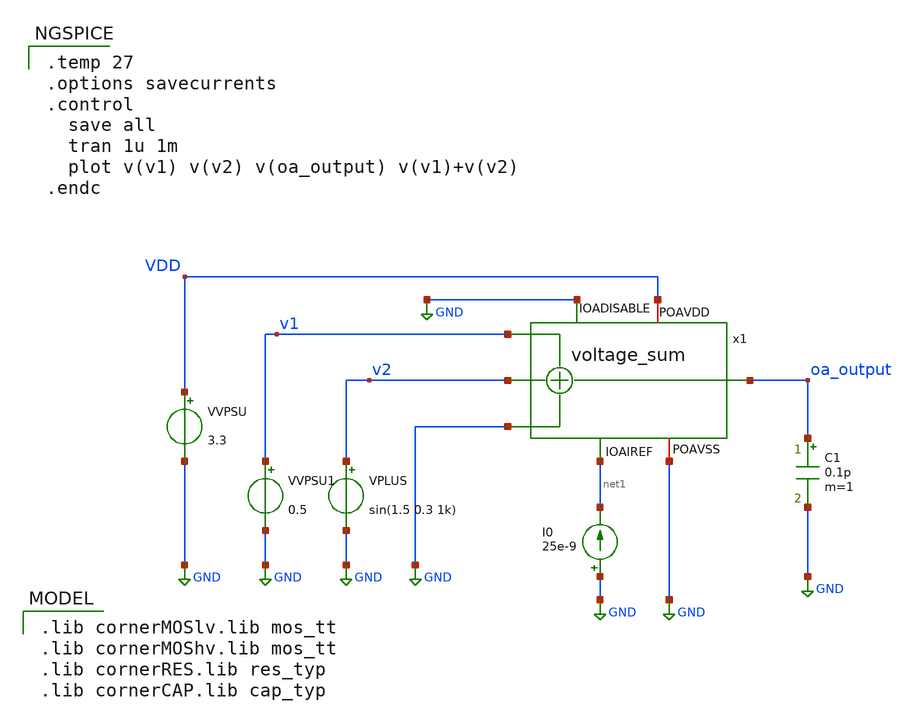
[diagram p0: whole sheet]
** sch_path: macros/voltage_controlled_resistors/macros/voltage_sum/testbenches/xschem/voltage_sum_tb_tran.sch
**.subckt voltage_sum_tb_tran
VVPSU VDD GND 3.3
I0 GND net1 25e-9
VPLUS v2 GND sin(1.5 0.3 1k)
C1 oa_output GND 0.1p m=1
x1 VDD net1 oa_output v1 GND GND v2 GND voltage_sum
VVPSU1 v1 GND 0.5
**** begin user architecture code

.lib cornerMOSlv.lib mos_tt
.lib cornerMOShv.lib mos_tt
.lib cornerRES.lib res_typ
.lib cornerCAP.lib cap_typ



.temp 27
.options savecurrents
.control
  save all
  tran 1u 1m
  plot v(v1) v(v2) v(oa_output) v(v1)+v(v2)
.endc


**** end user architecture code
**.ends
.GLOBAL GND
.end
